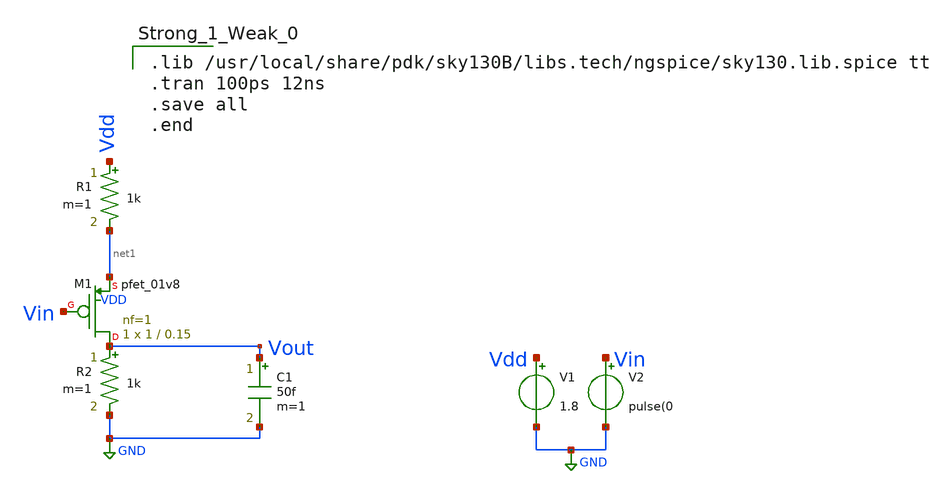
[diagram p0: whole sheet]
** sch_path: Xschem/pmos_test.sch
**.subckt pmos_test
XM1 Vout Vin net1 VDD sky130_fd_pr__pfet_01v8 L=0.15 W=1 nf=1 ad='int((nf+1)/2) * W/nf * 0.29' as='int((nf+2)/2) * W/nf * 0.29'
+ pd='2*int((nf+1)/2) * (W/nf + 0.29)' ps='2*int((nf+2)/2) * (W/nf + 0.29)' nrd='0.29 / W' nrs='0.29 / W'
+ sa=0 sb=0 sd=0 mult=1 m=1
R1 Vdd net1 1k m=1
C1 Vout GND 50f m=1
V1 Vdd GND 1.8
V2 Vin GND pulse(0
R2 Vout GND 1k m=1
**** begin user architecture code

.lib /usr/local/share/pdk/sky130B/libs.tech/ngspice/sky130.lib.spice tt
.tran 100ps 12ns
.save all
.end

**** end user architecture code
**.ends
.GLOBAL GND
.end
